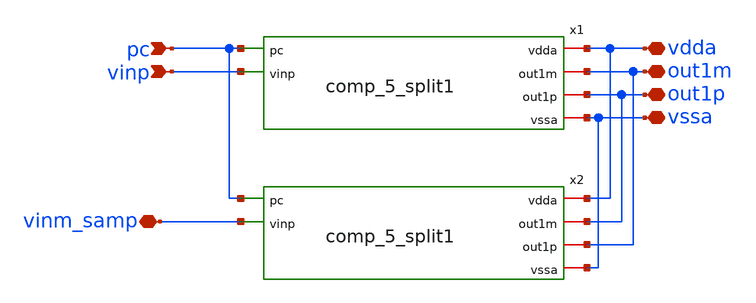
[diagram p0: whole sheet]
** sch_path: 5_Design/4_Layout/Team 5/xschem/comp_5_splitTop1.sch
**.subckt comp_5_splitTop1 pc vdda vssa vinp out1m out1p vinm_samp
*.ipin pc
*.iopin vdda
*.iopin vssa
*.ipin vinp
*.iopin out1m
*.iopin out1p
*.iopin vinm_samp
x1 vdda pc out1m out1p vinp vssa comp_5_split1
x2 vdda pc out1p out1m vinm_samp vssa comp_5_split1
**.ends

* expanding   symbol:  /foss/designs/comp_5_split1.sym # of pins=6
** sym_path: 5_Design/4_Layout/Team 5/xschem/comp_5_split1.sym
** sch_path: 5_Design/4_Layout/Team 5/xschem/comp_5_split1.sch
.subckt comp_5_split1 vdda pc out1m out1p vinp vssa
*.ipin pc
*.iopin vdda
*.iopin vssa
*.ipin vinp
*.iopin out1m
*.iopin out1p
XM2 out1m pc vdda vdda sg13_lv_pmos w=4u l=0.13u ng=1 m=1 mm_ok=1
XM1 out1m out1p vdda vdda sg13_lv_pmos w=4u l=0.13u ng=1 m=1 mm_ok=1
XM4 net2 out1p out1m vssa sg13_lv_nmos w=2u l=0.13u ng=1 m=1 mm_ok=1
XM7 net1 pc net2 vssa sg13_lv_nmos w=2u l=0.13u ng=1 m=1 mm_ok=1
XM8 vssa vinp net1 vssa sg13_lv_nmos w=2u l=1u ng=1 m=1 mm_ok=1
.ends

.end
